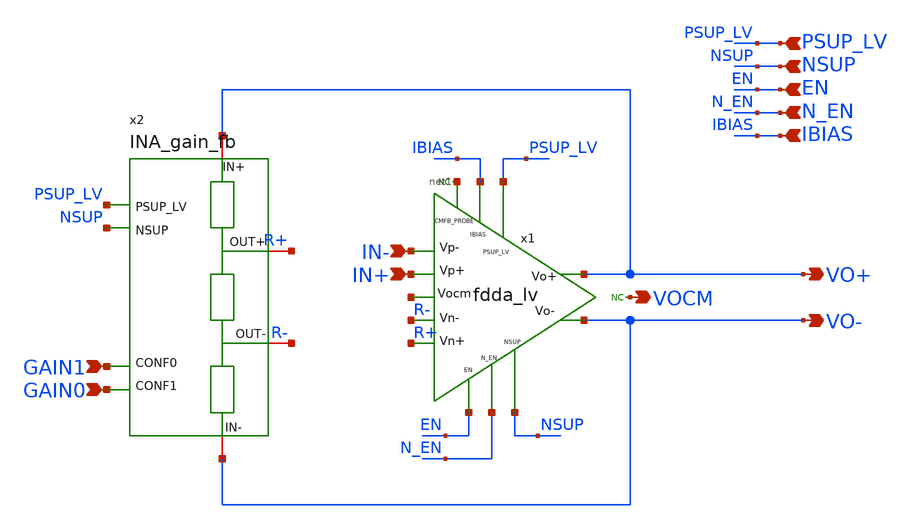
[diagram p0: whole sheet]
** sch_path: xschem/blocks/INA/INA.sch
**.subckt INA VO+ VO- IN+ IN- NSUP EN N_EN IBIAS PSUP_LV GAIN0 GAIN1 VOCM
*.opin VO+
*.opin VO-
*.ipin IN+
*.ipin IN-
*.ipin NSUP
*.ipin EN
*.ipin N_EN
*.ipin IBIAS
*.ipin PSUP_LV
*.ipin GAIN0
*.ipin GAIN1
*.opin VOCM
* noconn VOCM
* noconn #net1
x1 PSUP_LV IN- R- R+ IN+ VO+ VO- IBIAS N_EN EN NSUP net1 net2 fdda_lv
x2 VO+ R+ PSUP_LV NSUP GAIN0 GAIN1 R- VO- INA_gain_fb
**.ends
.end
